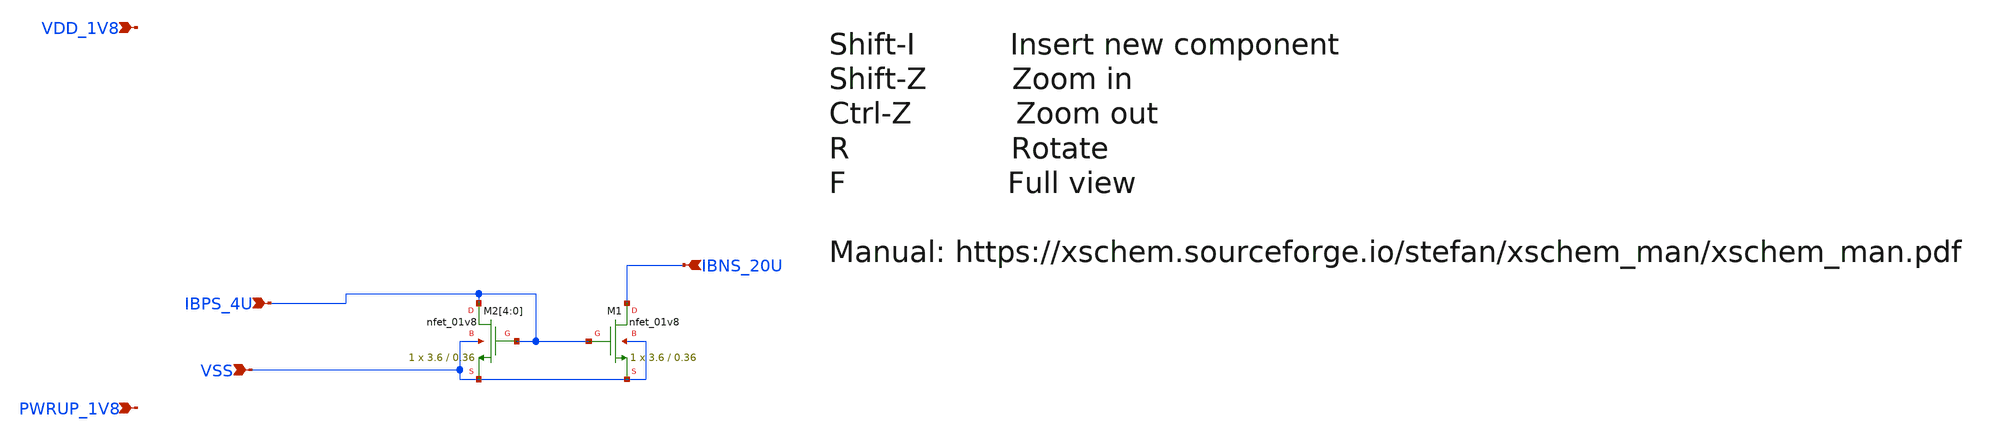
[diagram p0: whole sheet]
** sch_path: design/RPLY_TEST_SKY130NM/RPLY_TEST.sch
**.subckt RPLY_TEST VDD_1V8 VSS PWRUP_1V8 IBPS_4U IBNS_20U
*.ipin VDD_1V8
*.ipin VSS
*.ipin PWRUP_1V8
*.ipin IBPS_4U
*.ipin IBNS_20U
XM1 IBNS_20U IBPS_4U VSS VSS sky130_fd_pr__nfet_01v8 W=3.6 L=0.36 ad='int((2 + 1)/2) * 3.6 / 2 * 0.29'
+ pd='2*int((2 + 1)/2) * (3.6 / 2 + 0.29)' as='int((2 + 2)/2) * 3.6 / 2 * 0.29' ps='2*int((2 + 2)/2) * (3.6 / 2 + 0.29)'
+ nrd='0.29 / 3.6 ' nrs='0.29 / 3.6 ' sa=0 sb=0 sd=0 nf=2 mult=1
XM2[4] IBPS_4U IBPS_4U VSS VSS sky130_fd_pr__nfet_01v8 W=3.6 L=0.36 ad='int((2 + 1)/2) * 3.6 / 2 * 0.29'
+ pd='2*int((2 + 1)/2) * (3.6 / 2 + 0.29)' as='int((2 + 2)/2) * 3.6 / 2 * 0.29' ps='2*int((2 + 2)/2) * (3.6 / 2 + 0.29)'
+ nrd='0.29 / 3.6 ' nrs='0.29 / 3.6 ' sa=0 sb=0 sd=0 nf=2 mult=1
XM2[3] IBPS_4U IBPS_4U VSS VSS sky130_fd_pr__nfet_01v8 W=3.6 L=0.36 ad='int((2 + 1)/2) * 3.6 / 2 * 0.29'
+ pd='2*int((2 + 1)/2) * (3.6 / 2 + 0.29)' as='int((2 + 2)/2) * 3.6 / 2 * 0.29' ps='2*int((2 + 2)/2) * (3.6 / 2 + 0.29)'
+ nrd='0.29 / 3.6 ' nrs='0.29 / 3.6 ' sa=0 sb=0 sd=0 nf=2 mult=1
XM2[2] IBPS_4U IBPS_4U VSS VSS sky130_fd_pr__nfet_01v8 W=3.6 L=0.36 ad='int((2 + 1)/2) * 3.6 / 2 * 0.29'
+ pd='2*int((2 + 1)/2) * (3.6 / 2 + 0.29)' as='int((2 + 2)/2) * 3.6 / 2 * 0.29' ps='2*int((2 + 2)/2) * (3.6 / 2 + 0.29)'
+ nrd='0.29 / 3.6 ' nrs='0.29 / 3.6 ' sa=0 sb=0 sd=0 nf=2 mult=1
XM2[1] IBPS_4U IBPS_4U VSS VSS sky130_fd_pr__nfet_01v8 W=3.6 L=0.36 ad='int((2 + 1)/2) * 3.6 / 2 * 0.29'
+ pd='2*int((2 + 1)/2) * (3.6 / 2 + 0.29)' as='int((2 + 2)/2) * 3.6 / 2 * 0.29' ps='2*int((2 + 2)/2) * (3.6 / 2 + 0.29)'
+ nrd='0.29 / 3.6 ' nrs='0.29 / 3.6 ' sa=0 sb=0 sd=0 nf=2 mult=1
XM2[0] IBPS_4U IBPS_4U VSS VSS sky130_fd_pr__nfet_01v8 W=3.6 L=0.36 ad='int((2 + 1)/2) * 3.6 / 2 * 0.29'
+ pd='2*int((2 + 1)/2) * (3.6 / 2 + 0.29)' as='int((2 + 2)/2) * 3.6 / 2 * 0.29' ps='2*int((2 + 2)/2) * (3.6 / 2 + 0.29)'
+ nrd='0.29 / 3.6 ' nrs='0.29 / 3.6 ' sa=0 sb=0 sd=0 nf=2 mult=1
**.ends
.end
